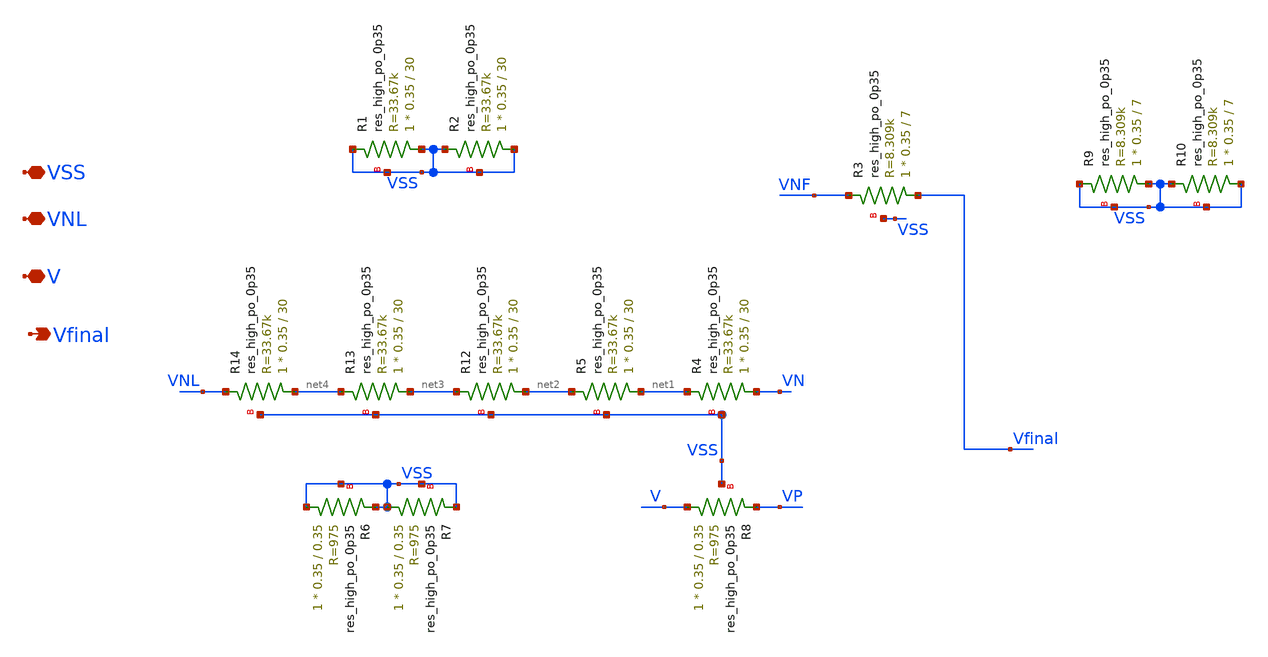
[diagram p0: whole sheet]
** sch_path: xschem/xschem_BGR_Top/untitled.sch
**.subckt untitled Vfinal VNL V VSS
*.opin Vfinal
*.iopin VNL
*.iopin V
*.iopin VSS
XR8 V VP VSS sky130_fd_pr__res_high_po_0p35 L=0.35 mult=1 m=1
XR3 Vfinal VNF VSS sky130_fd_pr__res_high_po_0p35 L=7 mult=1 m=1
XR4 VN net1 VSS sky130_fd_pr__res_high_po_0p35 L=30 mult=1 m=1
XR5 net1 net2 VSS sky130_fd_pr__res_high_po_0p35 L=30 mult=1 m=1
XR12 net2 net3 VSS sky130_fd_pr__res_high_po_0p35 L=30 mult=1 m=1
XR13 net3 net4 VSS sky130_fd_pr__res_high_po_0p35 L=30 mult=1 m=1
XR14 net4 VNL VSS sky130_fd_pr__res_high_po_0p35 L=30 mult=1 m=1
XR1 VSS VSS VSS sky130_fd_pr__res_high_po_0p35 L=30 mult=1 m=1
XR2 VSS VSS VSS sky130_fd_pr__res_high_po_0p35 L=30 mult=1 m=1
XR6 VSS VSS VSS sky130_fd_pr__res_high_po_0p35 L=0.35 mult=1 m=1
XR7 VSS VSS VSS sky130_fd_pr__res_high_po_0p35 L=0.35 mult=1 m=1
XR9 VSS VSS VSS sky130_fd_pr__res_high_po_0p35 L=7 mult=1 m=1
XR10 VSS VSS VSS sky130_fd_pr__res_high_po_0p35 L=7 mult=1 m=1
**.ends
.end
